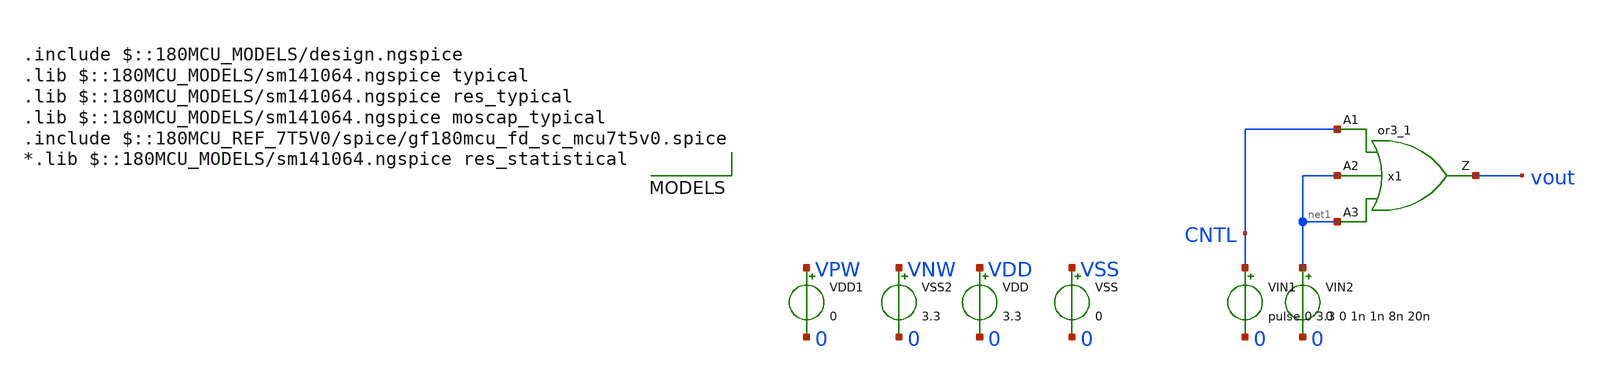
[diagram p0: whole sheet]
** sch_path: xschem/std_cell/tb_fiiles/Test_or3.sch
**.subckt Test_or3
x1 CNTL net1 net1 vout VDD VNW VPW VSS gf180mcu_fd_sc_mcu7t5v0__or3_1
VIN1 CNTL 0 pulse 0 3.3 0 1n 1n 8n 20n
VIN2 net1 0 0
VDD VDD 0 3.3
VSS VSS 0 0
VDD1 VPW 0 0
VSS2 VNW 0 3.3
**** begin user architecture code

.include $::180MCU_MODELS/design.ngspice
.lib $::180MCU_MODELS/sm141064.ngspice typical
.lib $::180MCU_MODELS/sm141064.ngspice res_typical
.lib $::180MCU_MODELS/sm141064.ngspice moscap_typical
.include $::180MCU_REF_7T5V0/spice/gf180mcu_fd_sc_mcu7t5v0.spice
*.lib $::180MCU_MODELS/sm141064.ngspice res_statistical





.control
	tran 0.1n 5n
	*dc vin1 0 3.3 0.1
	plot v(CNTL) V(vout)
	plot v(vout)
	write test_and.raw

.endc
.save all




**** end user architecture code
**.ends
.end
